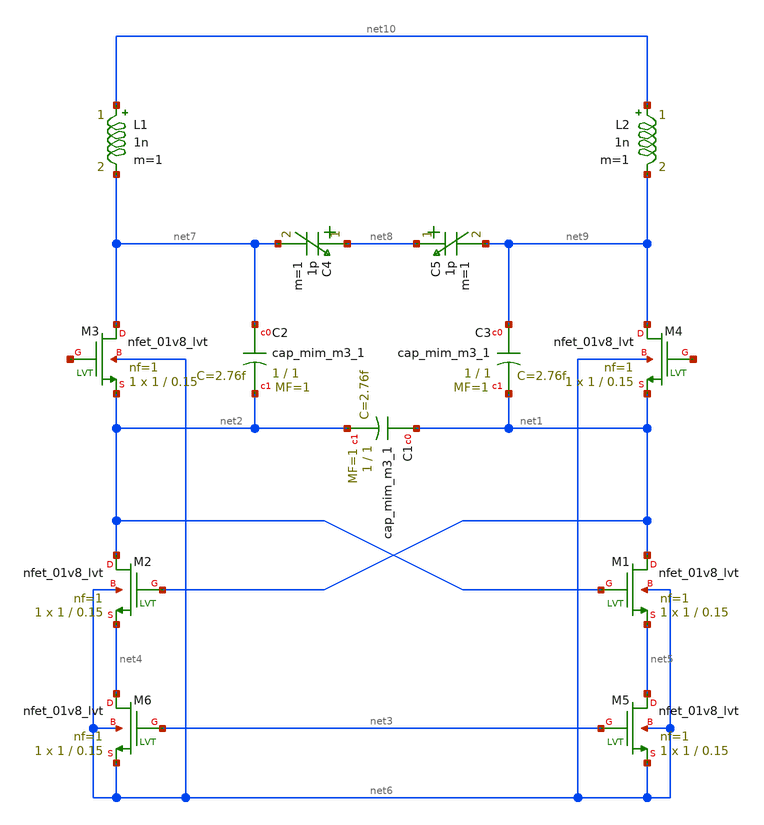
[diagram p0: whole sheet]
** sch_path: design/lc_oscillator_8ghz/lc_oscillator_8ghz.sch
**.subckt lc_oscillator_8ghz
XM1 net1 net2 net5 net6 sky130_fd_pr__nfet_01v8_lvt L=0.15 W=1 nf=1 ad='int((nf+1)/2) * W/nf * 0.29'
+ as='int((nf+2)/2) * W/nf * 0.29' pd='2*int((nf+1)/2) * (W/nf + 0.29)' ps='2*int((nf+2)/2) * (W/nf + 0.29)'
+ nrd='0.29 / W' nrs='0.29 / W' sa=0 sb=0 sd=0 mult=1 m=1
XM2 net2 net1 net4 net6 sky130_fd_pr__nfet_01v8_lvt L=0.15 W=1 nf=1 ad='int((nf+1)/2) * W/nf * 0.29'
+ as='int((nf+2)/2) * W/nf * 0.29' pd='2*int((nf+1)/2) * (W/nf + 0.29)' ps='2*int((nf+2)/2) * (W/nf + 0.29)'
+ nrd='0.29 / W' nrs='0.29 / W' sa=0 sb=0 sd=0 mult=1 m=1
XC1 net1 net2 sky130_fd_pr__cap_mim_m3_1 W=1 L=1 MF=1 m=1
XC2 net7 net2 sky130_fd_pr__cap_mim_m3_1 W=1 L=1 MF=1 m=1
XC3 net9 net1 sky130_fd_pr__cap_mim_m3_1 W=1 L=1 MF=1 m=1
XM3 net7 net11 net2 net6 sky130_fd_pr__nfet_01v8_lvt L=0.15 W=1 nf=1 ad='int((nf+1)/2) * W/nf * 0.29'
+ as='int((nf+2)/2) * W/nf * 0.29' pd='2*int((nf+1)/2) * (W/nf + 0.29)' ps='2*int((nf+2)/2) * (W/nf + 0.29)'
+ nrd='0.29 / W' nrs='0.29 / W' sa=0 sb=0 sd=0 mult=1 m=1
XM4 net9 net12 net1 net6 sky130_fd_pr__nfet_01v8_lvt L=0.15 W=1 nf=1 ad='int((nf+1)/2) * W/nf * 0.29'
+ as='int((nf+2)/2) * W/nf * 0.29' pd='2*int((nf+1)/2) * (W/nf + 0.29)' ps='2*int((nf+2)/2) * (W/nf + 0.29)'
+ nrd='0.29 / W' nrs='0.29 / W' sa=0 sb=0 sd=0 mult=1 m=1
XM5 net5 net3 net6 net6 sky130_fd_pr__nfet_01v8_lvt L=0.15 W=1 nf=1 ad='int((nf+1)/2) * W/nf * 0.29'
+ as='int((nf+2)/2) * W/nf * 0.29' pd='2*int((nf+1)/2) * (W/nf + 0.29)' ps='2*int((nf+2)/2) * (W/nf + 0.29)'
+ nrd='0.29 / W' nrs='0.29 / W' sa=0 sb=0 sd=0 mult=1 m=1
XM6 net4 net3 net6 net6 sky130_fd_pr__nfet_01v8_lvt L=0.15 W=1 nf=1 ad='int((nf+1)/2) * W/nf * 0.29'
+ as='int((nf+2)/2) * W/nf * 0.29' pd='2*int((nf+1)/2) * (W/nf + 0.29)' ps='2*int((nf+2)/2) * (W/nf + 0.29)'
+ nrd='0.29 / W' nrs='0.29 / W' sa=0 sb=0 sd=0 mult=1 m=1
C4 net8 net7 1p m=1
C5 net8 net9 1p m=1
L1 net10 net7 1n m=1
L2 net10 net9 1n m=1
**.ends
.end
